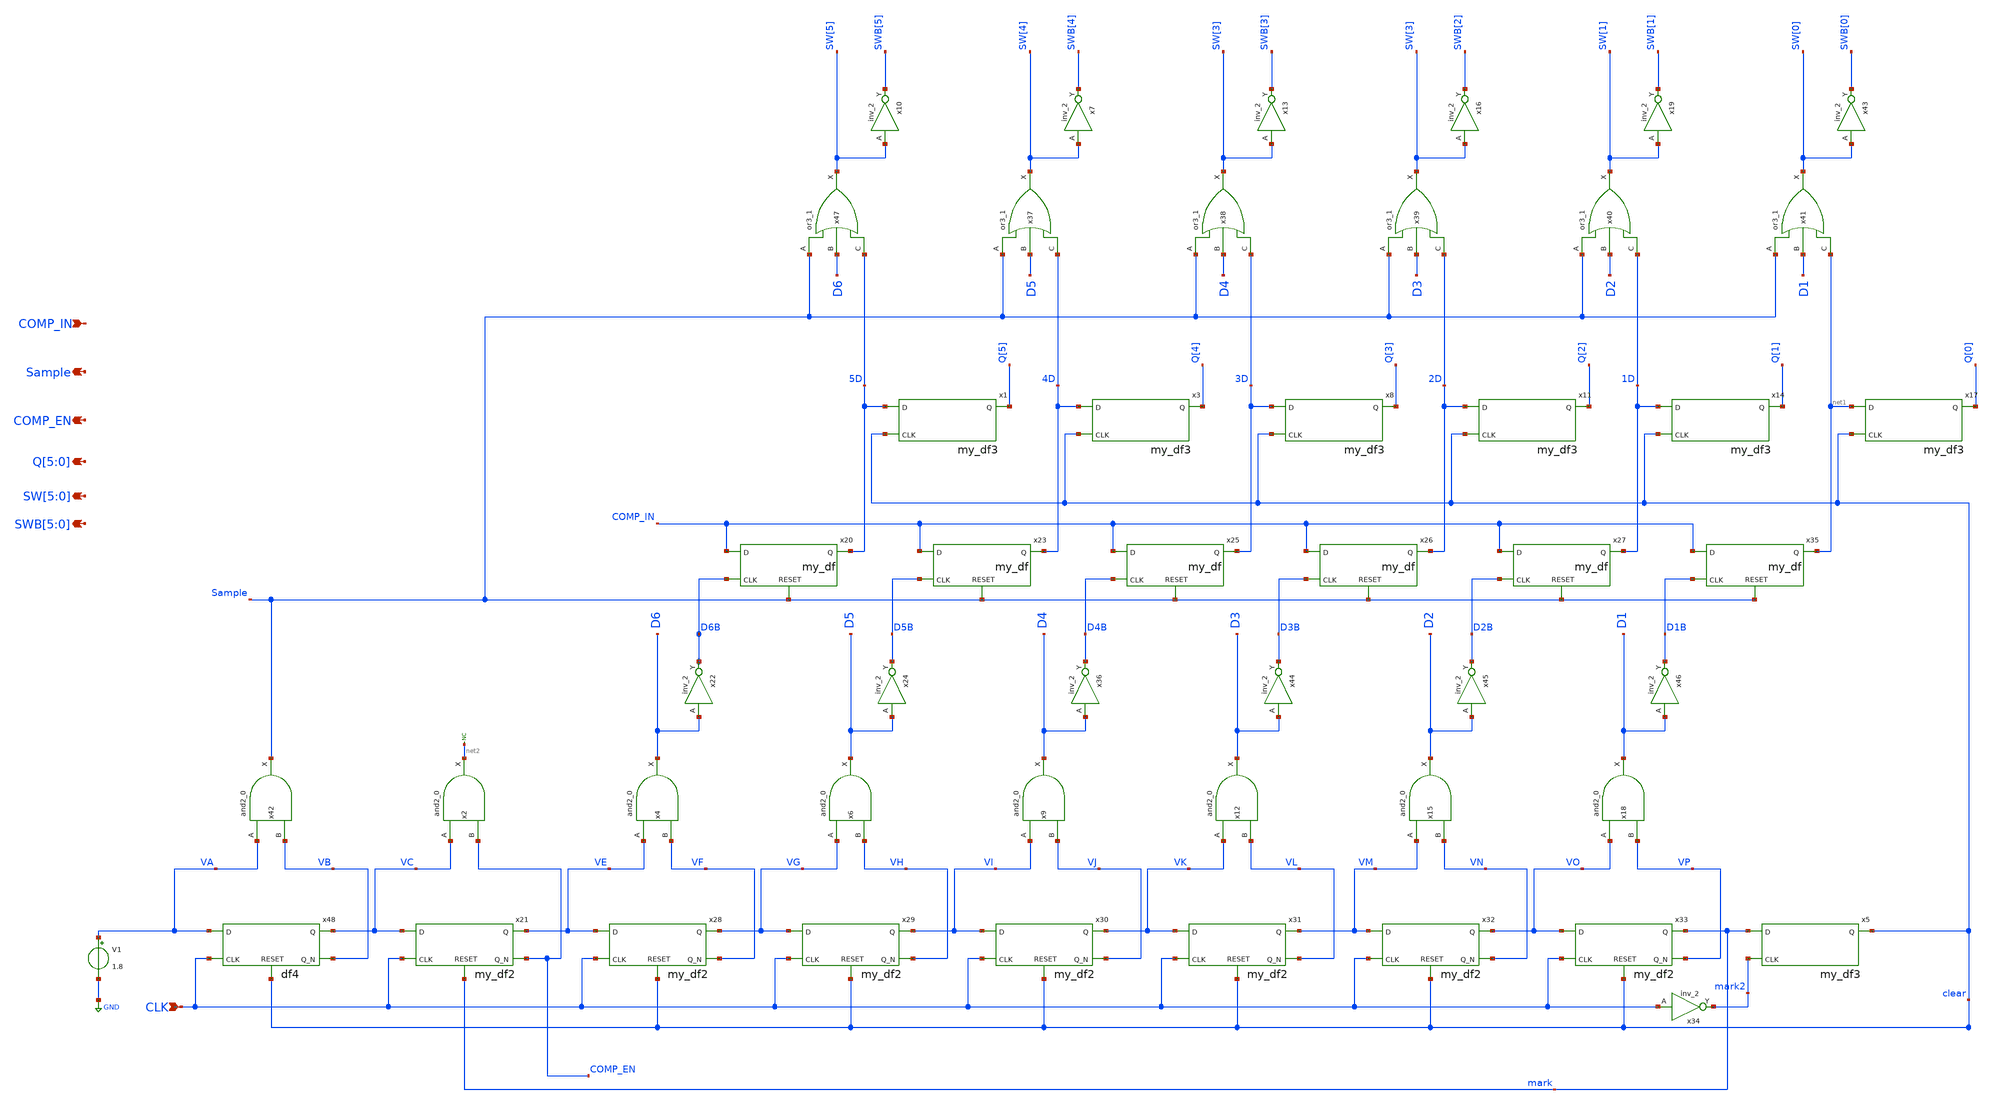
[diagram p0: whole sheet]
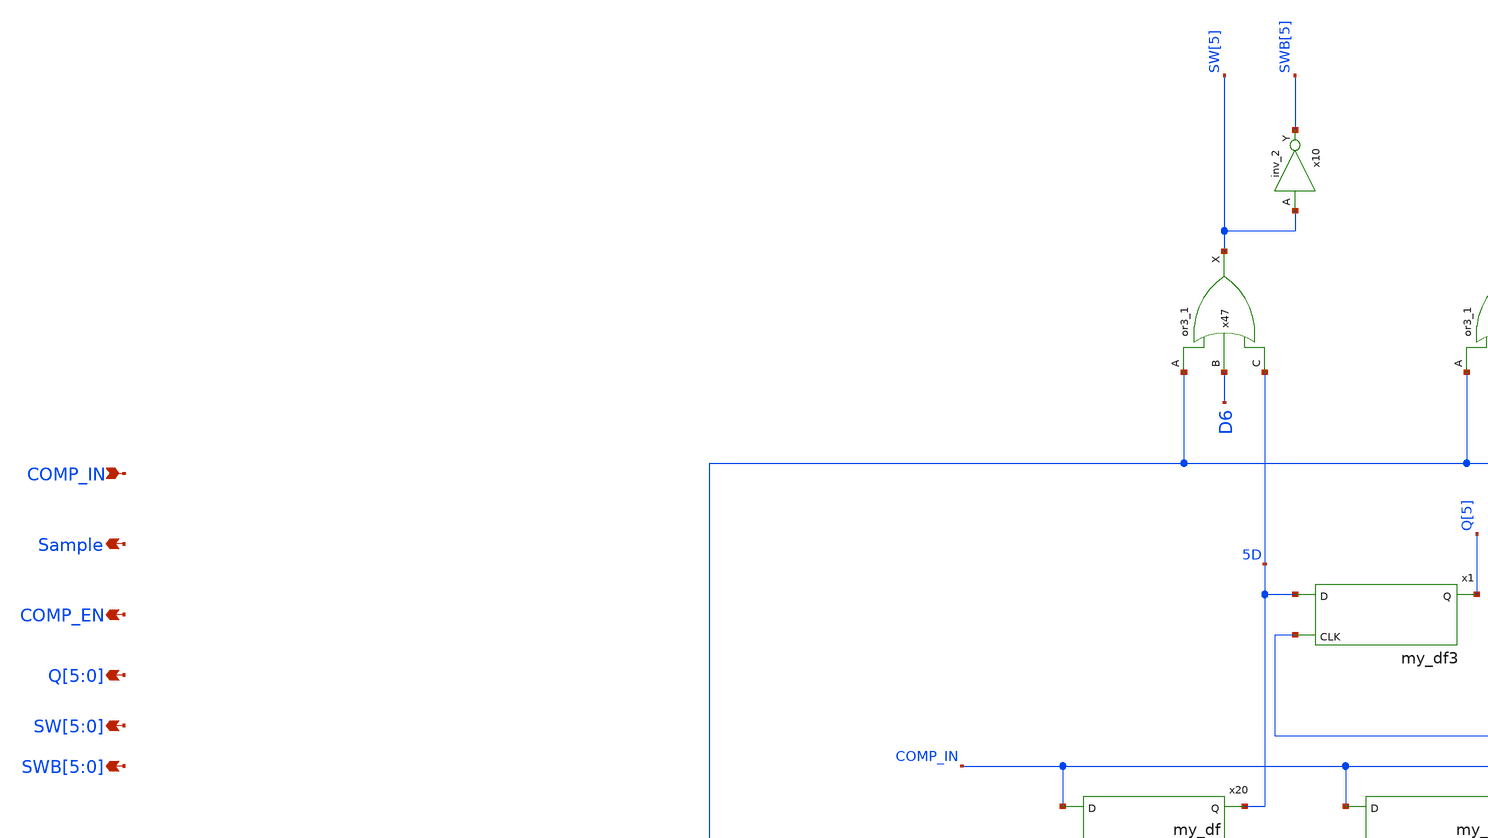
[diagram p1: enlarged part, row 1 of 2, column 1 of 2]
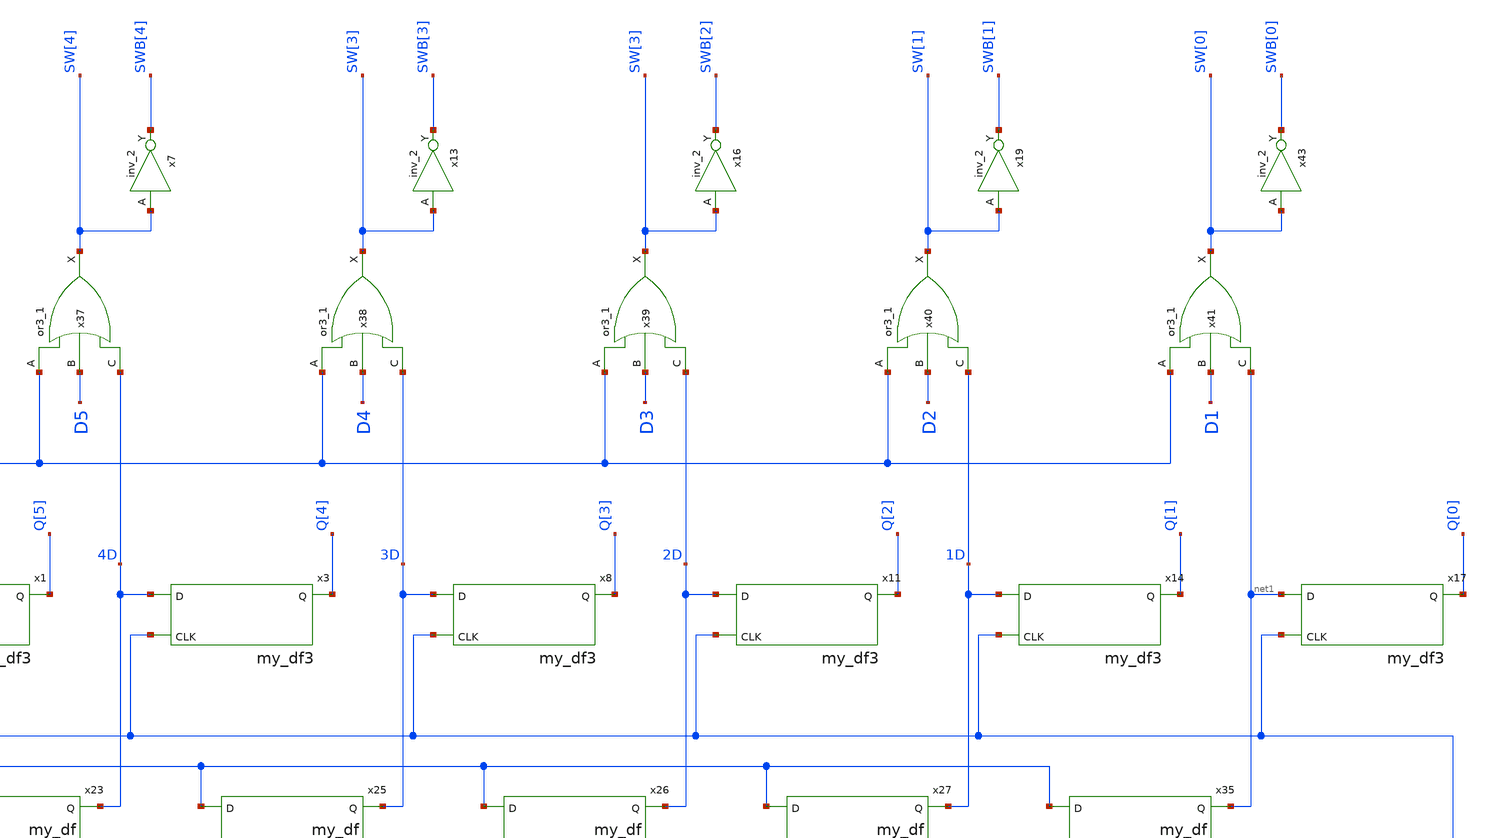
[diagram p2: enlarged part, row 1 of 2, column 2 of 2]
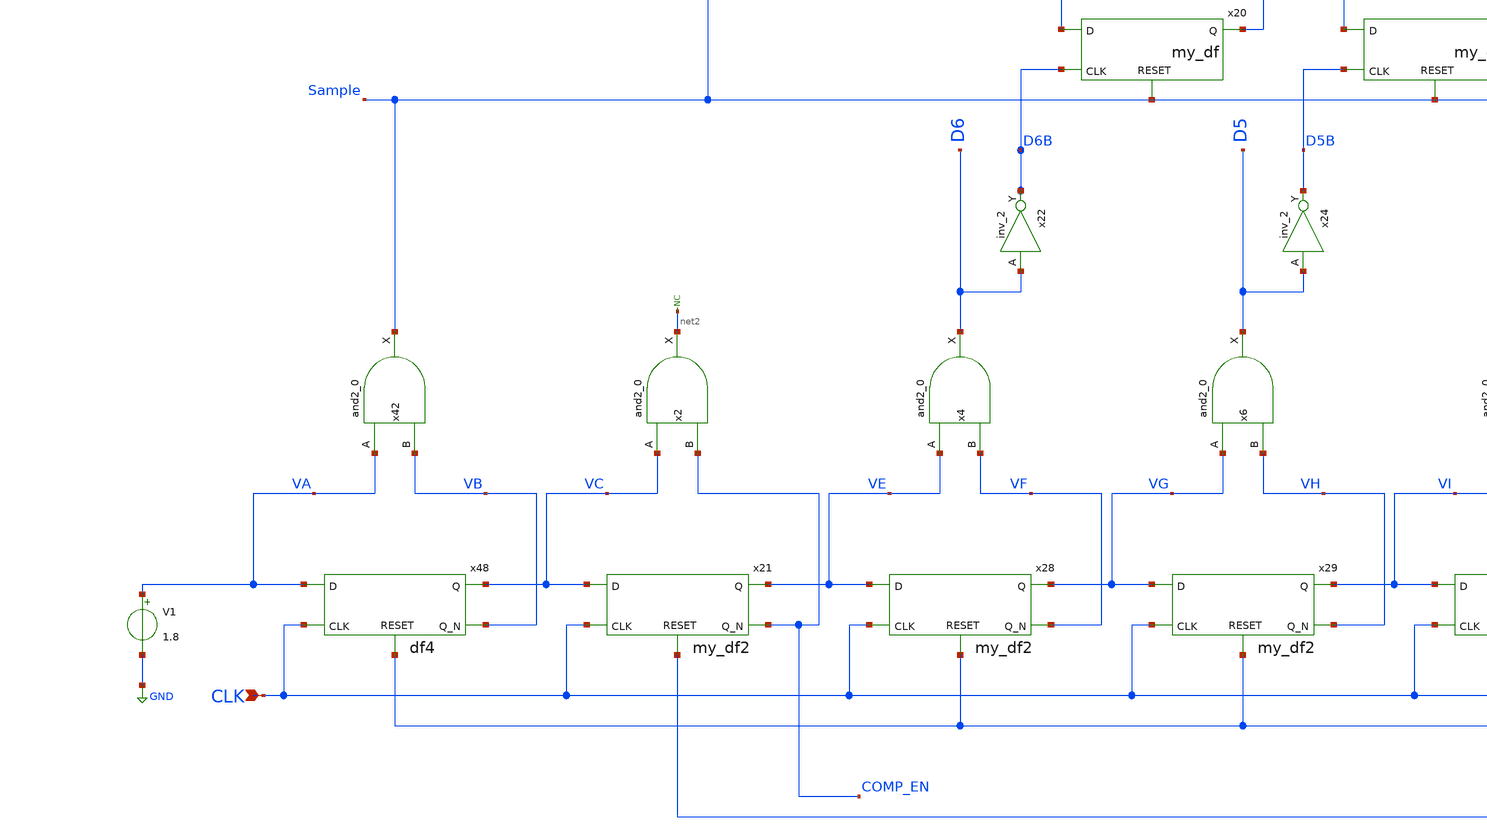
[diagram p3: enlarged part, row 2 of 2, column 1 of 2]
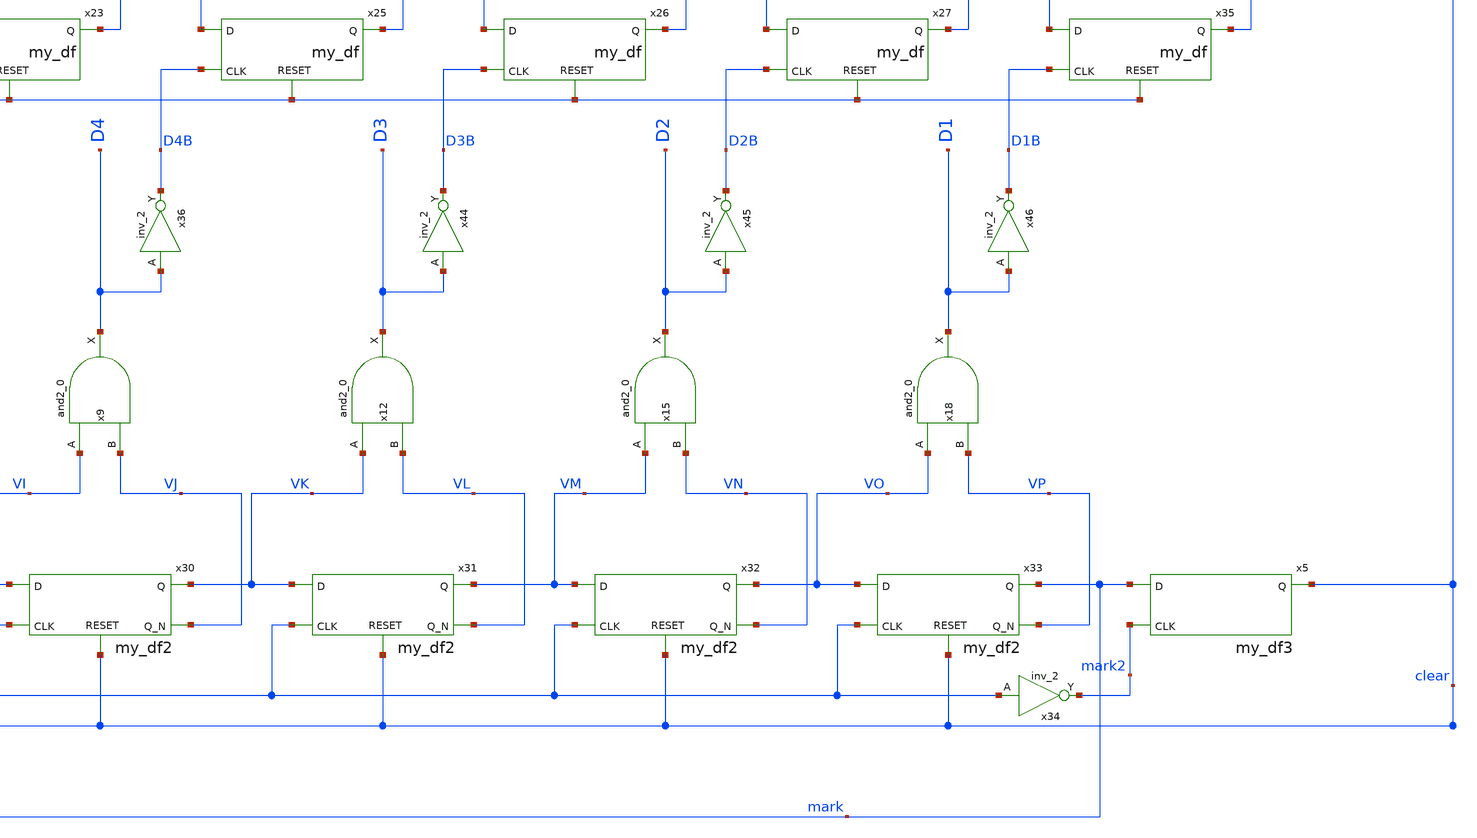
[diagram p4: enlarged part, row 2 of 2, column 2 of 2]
** sch_path: xschem/my_sar_logic.sch
**.subckt my_sar_logic Sample COMP_IN CLK COMP_EN Q[5],Q[4],Q[3],Q[2],Q[1],Q[0]
*+ SW[5],SW[4],SW[3],SW[2],SW[1],SW[0] SWB[5],SWB[4],SWB[3],SWB[2],SWB[1],SWB[0]
*.opin Sample
*.ipin COMP_IN
*.ipin CLK
*.opin COMP_EN
*.opin Q[5],Q[4],Q[3],Q[2],Q[1],Q[0]
*.opin SW[5],SW[4],SW[3],SW[2],SW[1],SW[0]
*.opin SWB[5],SWB[4],SWB[3],SWB[2],SWB[1],SWB[0]
x7 SW[4] GND GND VDD VDD SWB[4] sky130_fd_sc_hd__inv_2
x10 SW[5] GND GND VDD VDD SWB[5] sky130_fd_sc_hd__inv_2
x13 SW[3] GND GND VDD VDD SWB[3] sky130_fd_sc_hd__inv_2
x16 SW[3] GND GND VDD VDD SWB[2] sky130_fd_sc_hd__inv_2
x19 SW[1] GND GND VDD VDD SWB[1] sky130_fd_sc_hd__inv_2
x43 SW[0] GND GND VDD VDD SWB[0] sky130_fd_sc_hd__inv_2
x47 Sample D6 5D GND GND VDD VDD SW[5] sky130_fd_sc_hd__or3_1
x37 Sample D5 4D GND GND VDD VDD SW[4] sky130_fd_sc_hd__or3_1
x38 Sample D4 3D GND GND VDD VDD SW[3] sky130_fd_sc_hd__or3_1
x39 Sample D3 2D GND GND VDD VDD SW[3] sky130_fd_sc_hd__or3_1
x40 Sample D2 1D GND GND VDD VDD SW[1] sky130_fd_sc_hd__or3_1
x41 Sample D1 net1 GND GND VDD VDD SW[0] sky130_fd_sc_hd__or3_1
x20 D6B 5D COMP_IN Sample my_df
x23 D5B 4D COMP_IN Sample my_df
x25 D4B 3D COMP_IN Sample my_df
x26 D3B 2D COMP_IN Sample my_df
x27 D2B 1D COMP_IN Sample my_df
x35 D1B net1 COMP_IN Sample my_df
V1 VA GND 1.8
x22 D6 GND GND VDD VDD D6B sky130_fd_sc_hd__inv_2
x24 D5 GND GND VDD VDD D5B sky130_fd_sc_hd__inv_2
x36 D4 GND GND VDD VDD D4B sky130_fd_sc_hd__inv_2
x44 D3 GND GND VDD VDD D3B sky130_fd_sc_hd__inv_2
x45 D2 GND GND VDD VDD D2B sky130_fd_sc_hd__inv_2
x46 D1 GND GND VDD VDD D1B sky130_fd_sc_hd__inv_2
x42 VA VB GND GND VDD VDD Sample sky130_fd_sc_hd__and2_0
x2 VC COMP_EN GND GND VDD VDD net2 sky130_fd_sc_hd__and2_0
x4 VE VF GND GND VDD VDD D6 sky130_fd_sc_hd__and2_0
x6 VG VH GND GND VDD VDD D5 sky130_fd_sc_hd__and2_0
x9 VI VJ GND GND VDD VDD D4 sky130_fd_sc_hd__and2_0
x12 VK VL GND GND VDD VDD D3 sky130_fd_sc_hd__and2_0
x15 VM VN GND GND VDD VDD D2 sky130_fd_sc_hd__and2_0
x18 VO VP GND GND VDD VDD D1 sky130_fd_sc_hd__and2_0
x21 CLK VE VC COMP_EN mark my_df2
x28 CLK VG VE VF clear my_df2
x29 CLK VI VG VH clear my_df2
x30 CLK VK VI VJ clear my_df2
x31 CLK VM VK VL clear my_df2
x32 CLK VO VM VN clear my_df2
x33 CLK mark VO VP clear my_df2
x34 CLK GND GND VDD VDD mark2 sky130_fd_sc_hd__inv_2
x5 mark2 clear mark my_df3
x48 CLK VC VA VB clear df4
x1 clear Q[5] 5D my_df3
x3 clear Q[4] 4D my_df3
x8 clear Q[3] 3D my_df3
x11 clear Q[2] 2D my_df3
x14 clear Q[1] 1D my_df3
x17 clear Q[0] net1 my_df3
* noconn #net2
**.ends

* expanding   symbol:  my_df.sym # of pins=4
** sym_path: xschem/my_df.sym
** sch_path: xschem/my_df.sch
.subckt my_df CLK Q D RESET
*.ipin CLK
*.ipin D
*.ipin RESET
*.opin Q
x1 RESET GND GND VDD VDD net1 sky130_fd_sc_hd__inv_1
x3 CLK D net1 GND GND VDD VDD Q sky130_fd_sc_hd__dfrtp_1
.ends


* expanding   symbol:  my_df2.sym # of pins=5
** sym_path: xschem/my_df2.sym
** sch_path: xschem/my_df2.sch
.subckt my_df2 CLK Q D Q_N RESET
*.ipin CLK
*.ipin D
*.ipin RESET
*.opin Q
*.opin Q_N
x1 RESET GND GND VDD VDD net1 sky130_fd_sc_hd__inv_1
x2 CLK D net1 VDD GND GND VDD VDD Q Q_N sky130_fd_sc_hd__dfbbp_1
.ends


* expanding   symbol:  my_df3.sym # of pins=3
** sym_path: xschem/my_df3.sym
** sch_path: xschem/my_df3.sch
.subckt my_df3 CLK Q D
*.ipin CLK
*.ipin D
*.opin Q
x1 CLK D VDD GND GND VDD VDD Q sky130_fd_sc_hd__dfrtp_1
.ends


* expanding   symbol:  df4.sym # of pins=5
** sym_path: xschem/df4.sym
** sch_path: xschem/df4.sch
.subckt df4 CLK Q D Q_N RESET
*.ipin CLK
*.ipin D
*.ipin RESET
*.opin Q
*.opin Q_N
x2 RESET GND GND VDD VDD net1 sky130_fd_sc_hd__inv_1
x1 CLK D net1 GND GND VDD VDD Q Q_N sky130_fd_sc_hd__dfrbp_1
.ends

.GLOBAL GND
.GLOBAL VDD
.end
